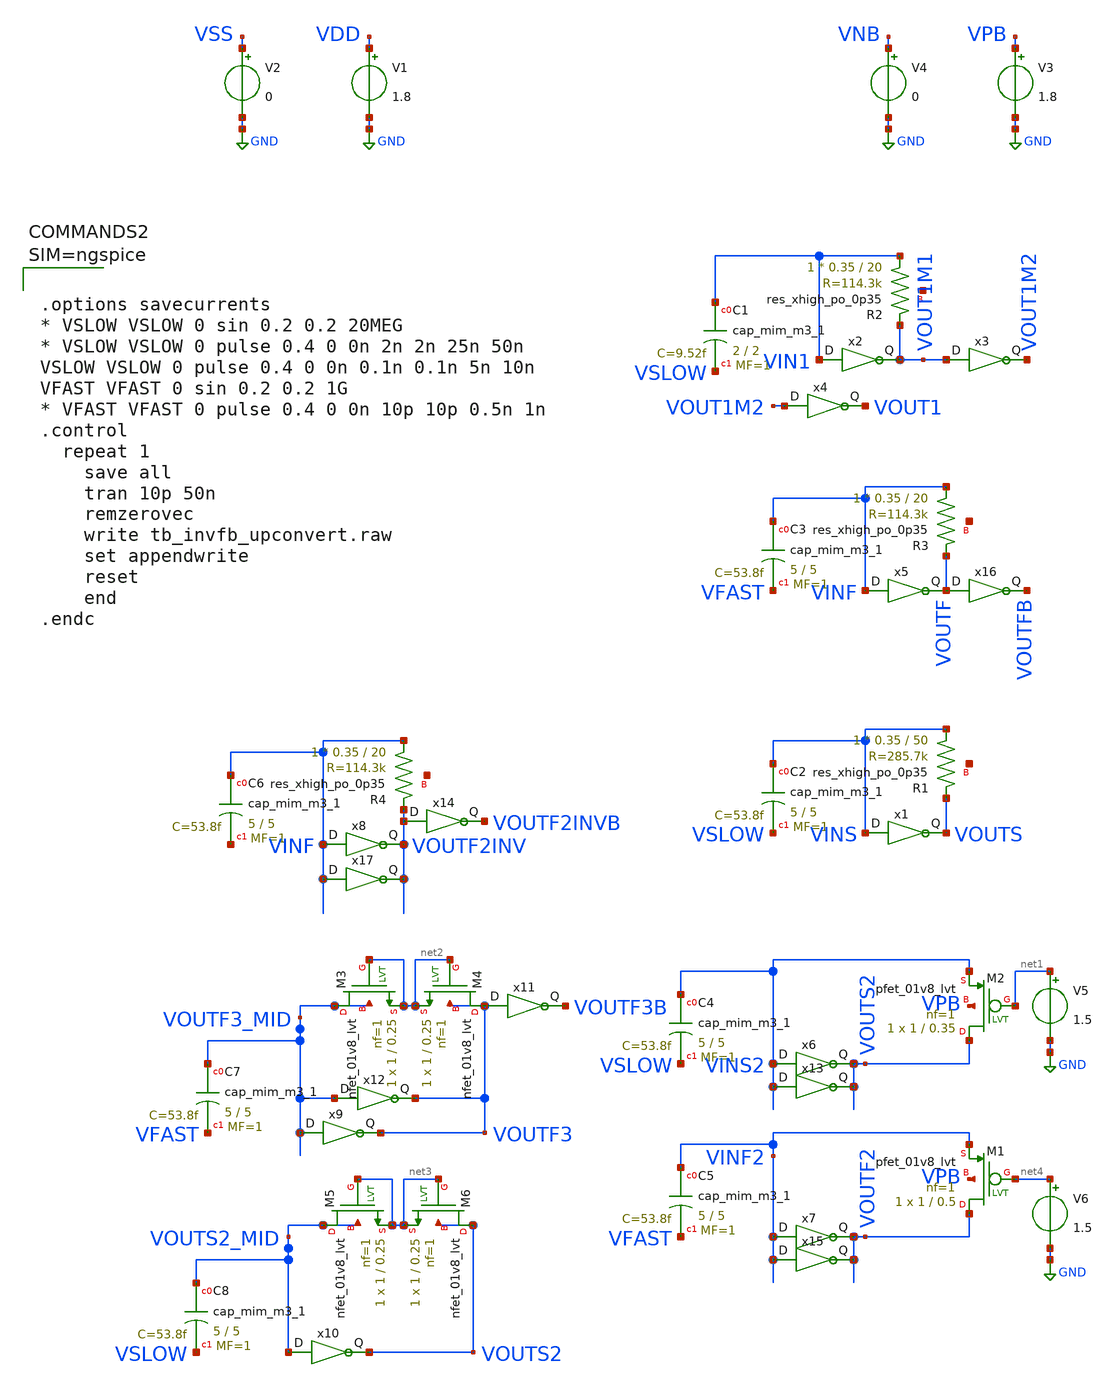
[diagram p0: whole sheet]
** sch_path: xschem/tb_invfb_upconvert.sch
**.subckt tb_invfb_upconvert
V1 VDD GND 1.8
V2 VSS GND 0
x3 VOUT1M1 VOUT1M2 VDD VSS pll_inv1
x1 VINS VOUTS VDD VSS pll_inv1
XR1 VINS VOUTS net5 sky130_fd_pr__res_xhigh_po_0p35 L=50 mult=1 m=1
XC2 VINS VSLOW sky130_fd_pr__cap_mim_m3_1 W=5 L=5 MF=1 m=1
V3 VPB GND 1.8
V4 VNB GND 0
XC1 VIN1 VSLOW sky130_fd_pr__cap_mim_m3_1 W=2 L=2 MF=1 m=1
x2 VIN1 VOUT1M1 VDD VSS pll_inv1
XR2 VIN1 VOUT1M1 net6 sky130_fd_pr__res_xhigh_po_0p35 L=20 mult=1 m=1
x4 VOUT1M2 VOUT1 VDD VSS pll_inv1
x5 VINF VOUTF VDD VSS pll_inv1
XR3 VINF VOUTF net7 sky130_fd_pr__res_xhigh_po_0p35 L=20 mult=1 m=1
XC3 VINF VFAST sky130_fd_pr__cap_mim_m3_1 W=5 L=5 MF=1 m=1
x6 VINS2 VOUTS2 VDD VSS pll_inv1
XC4 VINS2 VSLOW sky130_fd_pr__cap_mim_m3_1 W=5 L=5 MF=1 m=1
V5 net1 GND 1.5
XM2 VOUTS2 net1 VINS2 VPB sky130_fd_pr__pfet_01v8_lvt L=0.35 W=1 nf=1 ad='int((nf+1)/2) * W/nf * 0.29'
+ as='int((nf+2)/2) * W/nf * 0.29' pd='2*int((nf+1)/2) * (W/nf + 0.29)' ps='2*int((nf+2)/2) * (W/nf + 0.29)'
+ nrd='0.29 / W' nrs='0.29 / W' sa=0 sb=0 sd=0 mult=1 m=1
x7 VINF2 VOUTF2 VDD VSS pll_inv1
XC5 VINF2 VFAST sky130_fd_pr__cap_mim_m3_1 W=5 L=5 MF=1 m=1
V6 net4 GND 1.5
XM1 VOUTF2 net4 VINF2 VPB sky130_fd_pr__pfet_01v8_lvt L=0.5 W=1 nf=1 ad='int((nf+1)/2) * W/nf * 0.29'
+ as='int((nf+2)/2) * W/nf * 0.29' pd='2*int((nf+1)/2) * (W/nf + 0.29)' ps='2*int((nf+2)/2) * (W/nf + 0.29)'
+ nrd='0.29 / W' nrs='0.29 / W' sa=0 sb=0 sd=0 mult=1 m=1
x8 VINF VOUTF2INV VDD VSS pll_inv1
XR4 VINF VOUTF2INV net8 sky130_fd_pr__res_xhigh_po_0p35 L=20 mult=1 m=1
XC6 VINF net9 sky130_fd_pr__cap_mim_m3_1 W=5 L=5 MF=1 m=1
XC7 VOUTF3_MID VFAST sky130_fd_pr__cap_mim_m3_1 W=5 L=5 MF=1 m=1
XM3 VOUTF3_MID net2 net2 VOUTF3_MID sky130_fd_pr__nfet_01v8_lvt L=0.25 W=1 nf=1 ad='int((nf+1)/2) * W/nf * 0.29'
+ as='int((nf+2)/2) * W/nf * 0.29' pd='2*int((nf+1)/2) * (W/nf + 0.29)' ps='2*int((nf+2)/2) * (W/nf + 0.29)'
+ nrd='0.29 / W' nrs='0.29 / W' sa=0 sb=0 sd=0 mult=1 m=1
XM4 VOUTF3 net2 net2 VOUTF3 sky130_fd_pr__nfet_01v8_lvt L=0.25 W=1 nf=1 ad='int((nf+1)/2) * W/nf * 0.29'
+ as='int((nf+2)/2) * W/nf * 0.29' pd='2*int((nf+1)/2) * (W/nf + 0.29)' ps='2*int((nf+2)/2) * (W/nf + 0.29)'
+ nrd='0.29 / W' nrs='0.29 / W' sa=0 sb=0 sd=0 mult=1 m=1
x10 VOUTS2_MID VOUTS2 VDD VSS pll_inv1
XC8 VOUTS2_MID VSLOW sky130_fd_pr__cap_mim_m3_1 W=5 L=5 MF=1 m=1
XM5 VOUTS2_MID net3 net3 VOUTS2_MID sky130_fd_pr__nfet_01v8_lvt L=0.25 W=1 nf=1 ad='int((nf+1)/2) * W/nf * 0.29'
+ as='int((nf+2)/2) * W/nf * 0.29' pd='2*int((nf+1)/2) * (W/nf + 0.29)' ps='2*int((nf+2)/2) * (W/nf + 0.29)'
+ nrd='0.29 / W' nrs='0.29 / W' sa=0 sb=0 sd=0 mult=1 m=1
XM6 VOUTS2 net3 net3 VOUTS2 sky130_fd_pr__nfet_01v8_lvt L=0.25 W=1 nf=1 ad='int((nf+1)/2) * W/nf * 0.29'
+ as='int((nf+2)/2) * W/nf * 0.29' pd='2*int((nf+1)/2) * (W/nf + 0.29)' ps='2*int((nf+2)/2) * (W/nf + 0.29)'
+ nrd='0.29 / W' nrs='0.29 / W' sa=0 sb=0 sd=0 mult=1 m=1
x11 VOUTF3 VOUTF3B VDD VSS pll_inv1
x12 VOUTF3_MID VOUTF3 VDD VSS pll_inv1
x9 VOUTF3_MID VOUTF3 VDD VSS pll_inv1
x13 VINS2 VOUTS2 VDD VSS pll_inv1
x15 VINF2 VOUTF2 VDD VSS pll_inv1
x17 VINF VOUTF2INV VDD VSS pll_inv1
x14 VOUTF2INV VOUTF2INVB VDD VSS pll_inv1
x16 VOUTF VOUTFB VDD VSS pll_inv1
**** begin user architecture code

** opencircuitdesign pdks install
.lib $::SKYWATER_MODELS/sky130.lib.spice tt_mm





.options savecurrents
* VSLOW VSLOW 0 sin 0.2 0.2 20MEG
* VSLOW VSLOW 0 pulse 0.4 0 0n 2n 2n 25n 50n
VSLOW VSLOW 0 pulse 0.4 0 0n 0.1n 0.1n 5n 10n
VFAST VFAST 0 sin 0.2 0.2 1G
* VFAST VFAST 0 pulse 0.4 0 0n 10p 10p 0.5n 1n
.control
  repeat 1
    save all
    tran 10p 50n
    remzerovec
    write tb_invfb_upconvert.raw
    set appendwrite
    reset
    end
.endc



**** end user architecture code
**.ends

* expanding   symbol:  pll_inv1.sym # of pins=2
** sym_path: xschem/pll_inv1.sym
** sch_path: xschem/pll_inv1.sch
.subckt pll_inv1 D Q VDD VSS
*.opin Q
*.ipin D
*.ipin VDD
*.ipin VSS
XM3 Q D net1 net1 sky130_fd_pr__pfet_01v8_lvt L=0.5 W=1 nf=1 ad='int((nf+1)/2) * W/nf * 0.29' as='int((nf+2)/2) * W/nf * 0.29'
+ pd='2*int((nf+1)/2) * (W/nf + 0.29)' ps='2*int((nf+2)/2) * (W/nf + 0.29)' nrd='0.29 / W' nrs='0.29 / W'
+ sa=0 sb=0 sd=0 mult=1 m=1
vpwr VDD net1 0
.save i(vpwr)
XM1 Q D VSS VSS sky130_fd_pr__nfet_01v8_lvt L=0.25 W=0.5 nf=1 ad='int((nf+1)/2) * W/nf * 0.29' as='int((nf+2)/2) * W/nf * 0.29'
+ pd='2*int((nf+1)/2) * (W/nf + 0.29)' ps='2*int((nf+2)/2) * (W/nf + 0.29)' nrd='0.29 / W' nrs='0.29 / W'
+ sa=0 sb=0 sd=0 mult=1 m=1
.ends

.GLOBAL GND
.end
